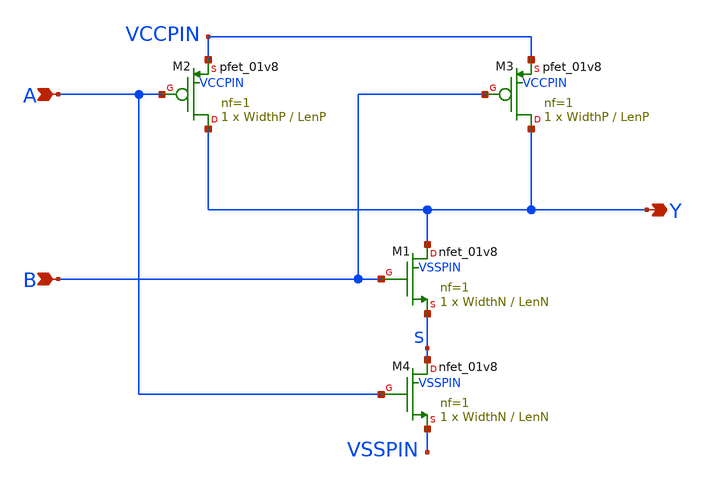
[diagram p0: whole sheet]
** sch_path: sky130A/xschem_libs/sky130_tests_ase/lvnand/schematic/lvnand.sch
* Copyright 2021 Stefan Frederik Schippers
* Licensed under the Apache License, Version 2.0 (the "License");
* you may not use this file except in compliance with the License.
* You may obtain a copy of the License at
* https://www.apache.org/licenses/LICENSE-2.0
* Unless required by applicable law or agreed to in writing, software
* distributed under the License is distributed on an "AS IS" BASIS,
* WITHOUT WARRANTIES OR CONDITIONS OF ANY KIND, either express or implied.
* See the License for the specific language governing permissions and
* limitations under the License.
**.subckt lvnand A B Y
*.ipin A
*.ipin B
*.opin Y
XM1 Y B S VSSPIN sky130_fd_pr__nfet_01v8 L=LenN W=WidthN nf=1 ad='int((nf+1)/2) * W/nf * 0.29' as='int((nf+2)/2) * W/nf * 0.29'
+ pd='2*int((nf+1)/2) * (W/nf + 0.29)' ps='2*int((nf+2)/2) * (W/nf + 0.29)' nrd='0.29 / W' nrs='0.29 / W'
+ sa=0 sb=0 sd=0 mult=1 m=1
XM2 Y A VCCPIN VCCPIN sky130_fd_pr__pfet_01v8 L=LenP W=WidthP nf=1 ad='int((1 + 1)/2) * WidthP / 1 * 0.29'
+ as='int((1 + 2)/2) * WidthP / 1 * 0.29' pd='2*int((1 + 1)/2) * (WidthP / 1 + 0.29)' ps='2*int((1 + 2)/2) * (WidthP / 1 + 0.29)'
+ nrd='0.29 / WidthP ' nrs='0.29 / WidthP ' sa=0 sb=0 sd=0 mult=1 m=1
XM3 Y B VCCPIN VCCPIN sky130_fd_pr__pfet_01v8 L=LenP W=WidthP nf=1 ad='int((1 + 1)/2) * WidthP / 1 * 0.29'
+ as='int((1 + 2)/2) * WidthP / 1 * 0.29' pd='2*int((1 + 1)/2) * (WidthP / 1 + 0.29)' ps='2*int((1 + 2)/2) * (WidthP / 1 + 0.29)'
+ nrd='0.29 / WidthP ' nrs='0.29 / WidthP ' sa=0 sb=0 sd=0 mult=1 m=1
XM4 S A VSSPIN VSSPIN sky130_fd_pr__nfet_01v8 L=LenN W=WidthN nf=1 ad='int((nf+1)/2) * W/nf * 0.29' as='int((nf+2)/2) * W/nf * 0.29'
+ pd='2*int((nf+1)/2) * (W/nf + 0.29)' ps='2*int((nf+2)/2) * (W/nf + 0.29)' nrd='0.29 / W' nrs='0.29 / W'
+ sa=0 sb=0 sd=0 mult=1 m=1
**.ends
**** begin user architecture code


vd d 0 0
vg g 0 0


**** end user architecture code
.end
